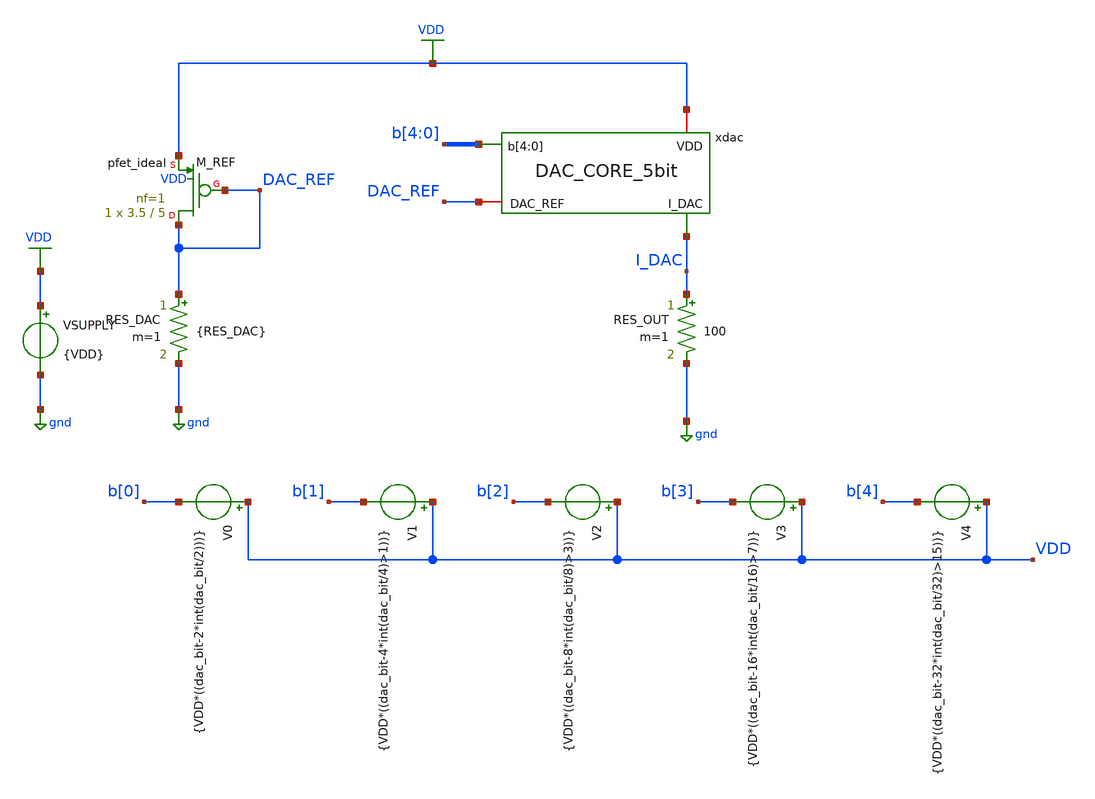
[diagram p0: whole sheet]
** sch_path: designs_backup/designs/lab2/DAC_CORE_5bit_test.sch
**.subckt DAC_CORE_5bit_test
RES_DAC DAC_REF gnd {RES_DAC} m=1
RES_OUT I_DAC gnd 100 m=1
V0 VDD b[0] {VDD*((dac_bit-2*int(dac_bit/2)))}
VSUPPLY VDD gnd {VDD}
V1 VDD b[1] {VDD*((dac_bit-4*int(dac_bit/4)>1))}
V2 VDD b[2] {VDD*((dac_bit-8*int(dac_bit/8)>3))}
V3 VDD b[3] {VDD*((dac_bit-16*int(dac_bit/16)>7))}
V4 VDD b[4] {VDD*((dac_bit-32*int(dac_bit/32)>15))}
XM_REF DAC_REF DAC_REF VDD VDD sky130_fd_pr__pfet_ideal L=5 W=3.5 nf=1 ad='int((1 + 1)/2) * 3.5 / 1 * 0.29'
+ as='int((1 + 2)/2) * 3.5 / 1 * 0.29' pd='2*int((1 + 1)/2) * (3.5 / 1 + 0.29)' ps='2*int((1 + 2)/2) * (3.5 / 1 + 0.29)'
+ nrd='0.29 / 3.5 ' nrs='0.29 / 3.5 ' sa=0 sb=0 sd=0 mult=1 m=1
xdac VDD DAC_REF I_DAC b[4] b[3] b[2] b[1] b[0] DAC_CORE_5bit
**** begin user architecture code

** opencircuitdesign pdks install
.lib $::SKYWATER_MODELS/sky130.lib.spice tt

* force include MC files
.include "$::SKYWATER_MODELS/parameters/montecarlo.spice"
.include "$::SKYWATER_MODELS/parameters/critical.spice"

* force mismatch/process params
.param mc_mm_switch = 0
.param mc_pr_switch = 0

* disable pfet_ideal from mismatch/process
.subckt sky130_fd_pr__pfet_ideal D G S B W=0.42 L=0.18  nf=1 ad='int((1 + 1)/2) * {W} / 1 * 0.29' as='int((1 + 2)/2) * {W} / 1 * 0.29'
+  pd='2*int((1 + 1)/2) * ({W} / 1 + 0.29)' ps='2*int((1 + 2)/2) * ({W} / 1 + 0.29)'   nrd='0.29 / {W}'
+ nrs='0.29 / {W}' sa=0 sb=0 sd=0 mult=1
  .param mc_mm_switch=0
  .param mc_pr_switch=0
  XIDEAL D G S B sky130_fd_pr__pfet_01v8 W={W} L={L}
  + nf={nf} ad={ad} as={as} pd={pd} ps={ps}
  + nrd={nrd} nrs={nrs} sa={sa} sb={sb} sd={sd} mult={mult}
.ends



.param VDD = 1.8
.param RES_DAC = 11.37k
.param dac_bit = 31
.options savecurrents

.control
  shell mkdir -p /foss/designs/lab2/results/2.10

  let dac_val = 31
  set corner = tt
  reset
  op
  let I_dac = @res_out[i] * 1e6
  echo -- corner= $corner  |  dac_bit= $&dac_val  |  I_DAC[uA]= $&I_dac -- >>
+ /foss/designs/lab2/results/2.10/DAC_corners.dat
  echo >> /foss/designs/lab2/results/2.10/DAC_corners.dat
.endc


**** end user architecture code
**.ends
.GLOBAL gnd
.GLOBAL VDD
.end
